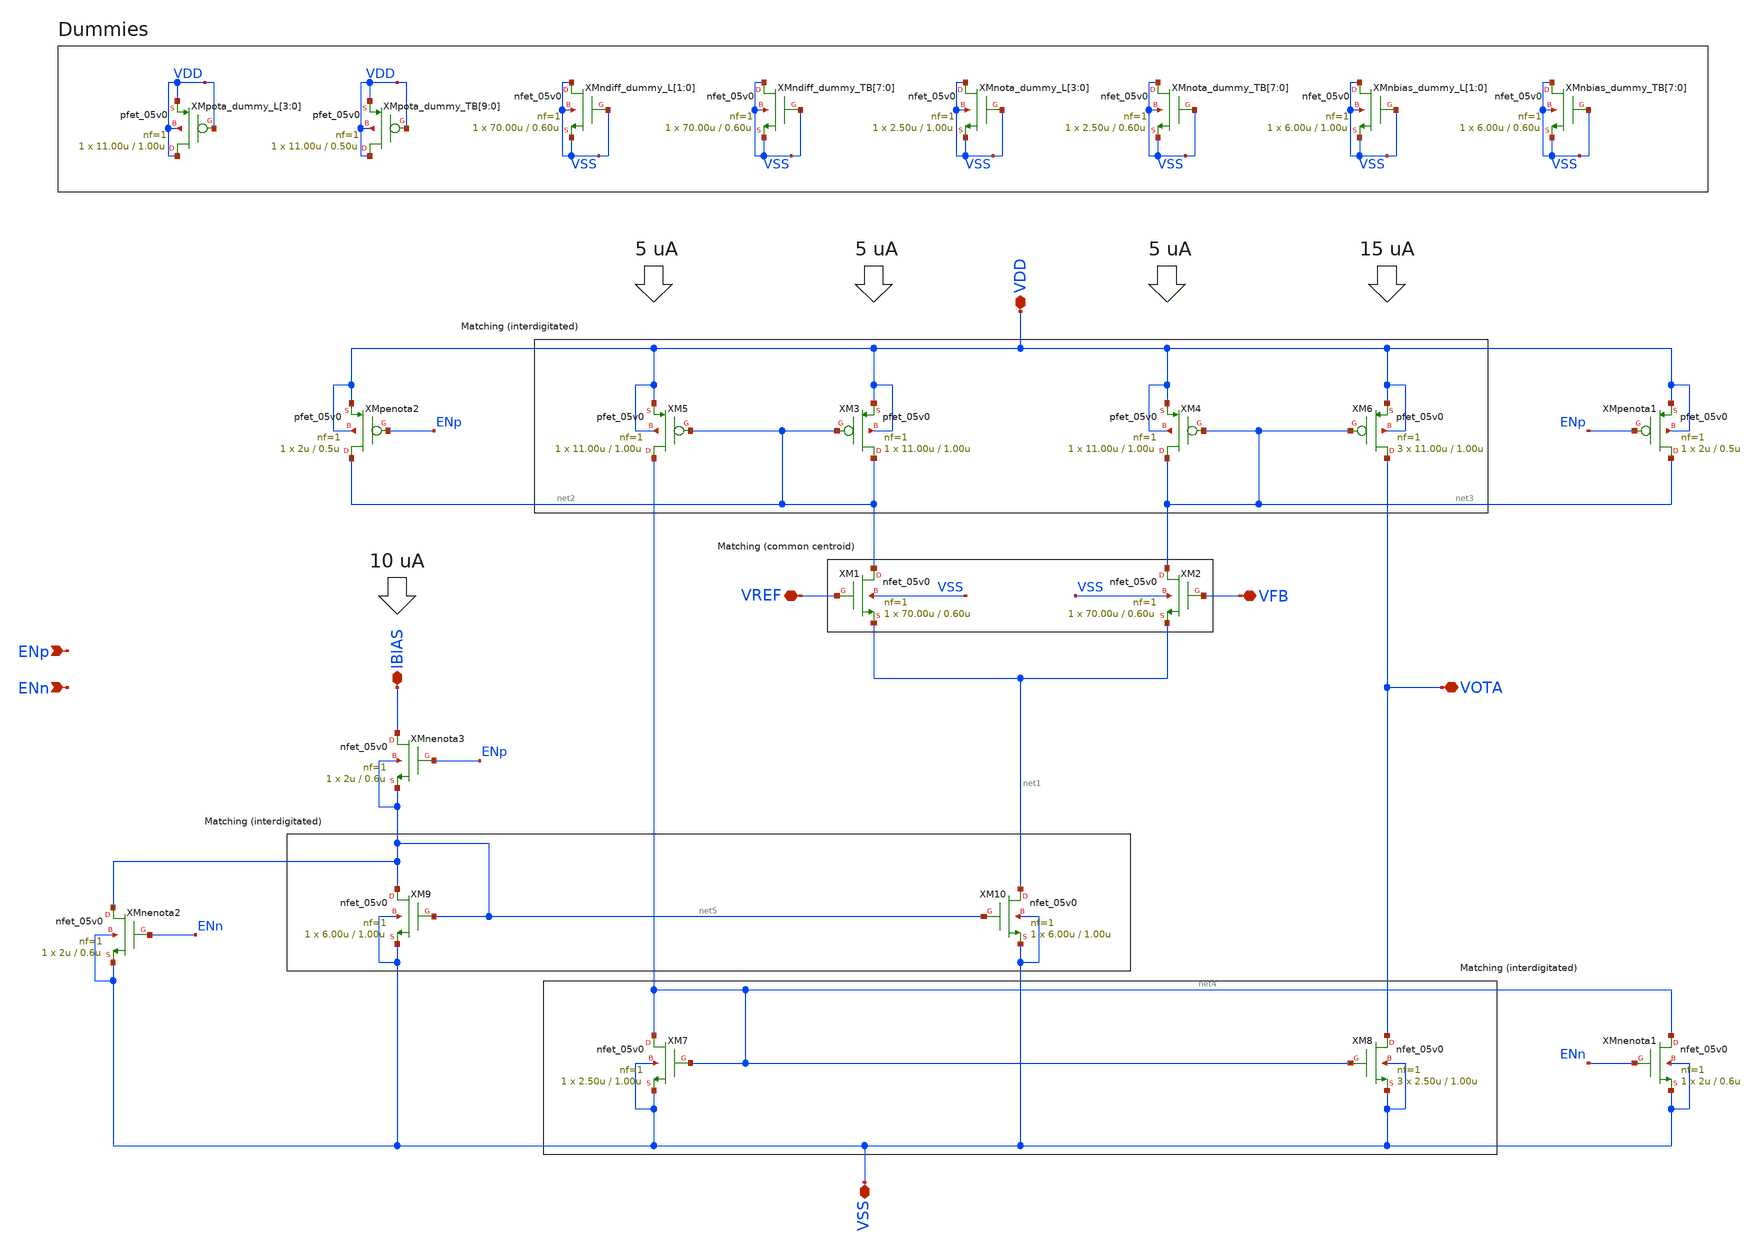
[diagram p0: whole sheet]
** sch_path: designs/libs/core_ldo/ldo_OTA/ldo_OTA.sch
**.subckt ldo_OTA VDD VSS VOTA VREF IBIAS VFB ENp ENn
*.iopin VDD
*.iopin VSS
*.iopin VOTA
*.iopin VREF
*.iopin IBIAS
*.iopin VFB
*.ipin ENp
*.ipin ENn
XM3 net2 net2 VDD VDD pfet_05v0 L=1.00u W=11.00u nf=1 ad='int((nf+1)/2) * W/nf * 0.18u' as='int((nf+2)/2) * W/nf * 0.18u'
+ pd='2*int((nf+1)/2) * (W/nf + 0.18u)' ps='2*int((nf+2)/2) * (W/nf + 0.18u)' nrd='0.18u / W' nrs='0.18u / W'
+ sa=0 sb=0 sd=0 m=1
XM4 net3 net3 VDD VDD pfet_05v0 L=1.00u W=11.00u nf=1 ad='int((nf+1)/2) * W/nf * 0.18u' as='int((nf+2)/2) * W/nf * 0.18u'
+ pd='2*int((nf+1)/2) * (W/nf + 0.18u)' ps='2*int((nf+2)/2) * (W/nf + 0.18u)' nrd='0.18u / W' nrs='0.18u / W'
+ sa=0 sb=0 sd=0 m=1
XM5 net4 net2 VDD VDD pfet_05v0 L=1.00u W=11.00u nf=1 ad='int((nf+1)/2) * W/nf * 0.18u' as='int((nf+2)/2) * W/nf * 0.18u'
+ pd='2*int((nf+1)/2) * (W/nf + 0.18u)' ps='2*int((nf+2)/2) * (W/nf + 0.18u)' nrd='0.18u / W' nrs='0.18u / W'
+ sa=0 sb=0 sd=0 m=1
XM6 VOTA net3 VDD VDD pfet_05v0 L=1.00u W=11.00u nf=1 ad='int((nf+1)/2) * W/nf * 0.18u' as='int((nf+2)/2) * W/nf * 0.18u'
+ pd='2*int((nf+1)/2) * (W/nf + 0.18u)' ps='2*int((nf+2)/2) * (W/nf + 0.18u)' nrd='0.18u / W' nrs='0.18u / W'
+ sa=0 sb=0 sd=0 m=3
XM9 net5 net5 VSS VSS nfet_05v0 L=1.00u W=6.00u nf=1 ad='int((nf+1)/2) * W/nf * 0.18u' as='int((nf+2)/2) * W/nf * 0.18u'
+ pd='2*int((nf+1)/2) * (W/nf + 0.18u)' ps='2*int((nf+2)/2) * (W/nf + 0.18u)' nrd='0.18u / W' nrs='0.18u / W'
+ sa=0 sb=0 sd=0 m=1
XM10 net1 net5 VSS VSS nfet_05v0 L=1.00u W=6.00u nf=1 ad='int((nf+1)/2) * W/nf * 0.18u' as='int((nf+2)/2) * W/nf * 0.18u'
+ pd='2*int((nf+1)/2) * (W/nf + 0.18u)' ps='2*int((nf+2)/2) * (W/nf + 0.18u)' nrd='0.18u / W' nrs='0.18u / W'
+ sa=0 sb=0 sd=0 m=1
XM7 net4 net4 VSS VSS nfet_05v0 L=1.00u W=2.50u nf=1 ad='int((nf+1)/2) * W/nf * 0.18u' as='int((nf+2)/2) * W/nf * 0.18u'
+ pd='2*int((nf+1)/2) * (W/nf + 0.18u)' ps='2*int((nf+2)/2) * (W/nf + 0.18u)' nrd='0.18u / W' nrs='0.18u / W'
+ sa=0 sb=0 sd=0 m=1
XM8 VOTA net4 VSS VSS nfet_05v0 L=1.00u W=2.50u nf=1 ad='int((nf+1)/2) * W/nf * 0.18u' as='int((nf+2)/2) * W/nf * 0.18u'
+ pd='2*int((nf+1)/2) * (W/nf + 0.18u)' ps='2*int((nf+2)/2) * (W/nf + 0.18u)' nrd='0.18u / W' nrs='0.18u / W'
+ sa=0 sb=0 sd=0 m=3
XM1 net2 VREF net1 VSS nfet_05v0 L=0.60u W=70.00u nf=1 ad='int((nf+1)/2) * W/nf * 0.18u' as='int((nf+2)/2) * W/nf * 0.18u'
+ pd='2*int((nf+1)/2) * (W/nf + 0.18u)' ps='2*int((nf+2)/2) * (W/nf + 0.18u)' nrd='0.18u / W' nrs='0.18u / W'
+ sa=0 sb=0 sd=0 m=1
XM2 net3 VFB net1 VSS nfet_05v0 L=0.60u W=70.00u nf=1 ad='int((nf+1)/2) * W/nf * 0.18u' as='int((nf+2)/2) * W/nf * 0.18u'
+ pd='2*int((nf+1)/2) * (W/nf + 0.18u)' ps='2*int((nf+2)/2) * (W/nf + 0.18u)' nrd='0.18u / W' nrs='0.18u / W'
+ sa=0 sb=0 sd=0 m=1
XMpota_dummy_L[3] VDD VDD VDD VDD pfet_05v0 L=1.00u W=11.00u nf=1 ad='int((nf+1)/2) * W/nf * 0.18u' as='int((nf+2)/2) * W/nf * 0.18u'
+ pd='2*int((nf+1)/2) * (W/nf + 0.18u)' ps='2*int((nf+2)/2) * (W/nf + 0.18u)' nrd='0.18u / W' nrs='0.18u / W'
+ sa=0 sb=0 sd=0 m=1
XMpota_dummy_L[2] VDD VDD VDD VDD pfet_05v0 L=1.00u W=11.00u nf=1 ad='int((nf+1)/2) * W/nf * 0.18u' as='int((nf+2)/2) * W/nf * 0.18u'
+ pd='2*int((nf+1)/2) * (W/nf + 0.18u)' ps='2*int((nf+2)/2) * (W/nf + 0.18u)' nrd='0.18u / W' nrs='0.18u / W'
+ sa=0 sb=0 sd=0 m=1
XMpota_dummy_L[1] VDD VDD VDD VDD pfet_05v0 L=1.00u W=11.00u nf=1 ad='int((nf+1)/2) * W/nf * 0.18u' as='int((nf+2)/2) * W/nf * 0.18u'
+ pd='2*int((nf+1)/2) * (W/nf + 0.18u)' ps='2*int((nf+2)/2) * (W/nf + 0.18u)' nrd='0.18u / W' nrs='0.18u / W'
+ sa=0 sb=0 sd=0 m=1
XMpota_dummy_L[0] VDD VDD VDD VDD pfet_05v0 L=1.00u W=11.00u nf=1 ad='int((nf+1)/2) * W/nf * 0.18u' as='int((nf+2)/2) * W/nf * 0.18u'
+ pd='2*int((nf+1)/2) * (W/nf + 0.18u)' ps='2*int((nf+2)/2) * (W/nf + 0.18u)' nrd='0.18u / W' nrs='0.18u / W'
+ sa=0 sb=0 sd=0 m=1
XMpota_dummy_TB[9] VDD VDD VDD VDD pfet_05v0 L=0.50u W=11.00u nf=1 ad='int((nf+1)/2) * W/nf * 0.18u'
+ as='int((nf+2)/2) * W/nf * 0.18u' pd='2*int((nf+1)/2) * (W/nf + 0.18u)' ps='2*int((nf+2)/2) * (W/nf + 0.18u)'
+ nrd='0.18u / W' nrs='0.18u / W' sa=0 sb=0 sd=0 m=1
XMpota_dummy_TB[8] VDD VDD VDD VDD pfet_05v0 L=0.50u W=11.00u nf=1 ad='int((nf+1)/2) * W/nf * 0.18u'
+ as='int((nf+2)/2) * W/nf * 0.18u' pd='2*int((nf+1)/2) * (W/nf + 0.18u)' ps='2*int((nf+2)/2) * (W/nf + 0.18u)'
+ nrd='0.18u / W' nrs='0.18u / W' sa=0 sb=0 sd=0 m=1
XMpota_dummy_TB[7] VDD VDD VDD VDD pfet_05v0 L=0.50u W=11.00u nf=1 ad='int((nf+1)/2) * W/nf * 0.18u'
+ as='int((nf+2)/2) * W/nf * 0.18u' pd='2*int((nf+1)/2) * (W/nf + 0.18u)' ps='2*int((nf+2)/2) * (W/nf + 0.18u)'
+ nrd='0.18u / W' nrs='0.18u / W' sa=0 sb=0 sd=0 m=1
XMpota_dummy_TB[6] VDD VDD VDD VDD pfet_05v0 L=0.50u W=11.00u nf=1 ad='int((nf+1)/2) * W/nf * 0.18u'
+ as='int((nf+2)/2) * W/nf * 0.18u' pd='2*int((nf+1)/2) * (W/nf + 0.18u)' ps='2*int((nf+2)/2) * (W/nf + 0.18u)'
+ nrd='0.18u / W' nrs='0.18u / W' sa=0 sb=0 sd=0 m=1
XMpota_dummy_TB[5] VDD VDD VDD VDD pfet_05v0 L=0.50u W=11.00u nf=1 ad='int((nf+1)/2) * W/nf * 0.18u'
+ as='int((nf+2)/2) * W/nf * 0.18u' pd='2*int((nf+1)/2) * (W/nf + 0.18u)' ps='2*int((nf+2)/2) * (W/nf + 0.18u)'
+ nrd='0.18u / W' nrs='0.18u / W' sa=0 sb=0 sd=0 m=1
XMpota_dummy_TB[4] VDD VDD VDD VDD pfet_05v0 L=0.50u W=11.00u nf=1 ad='int((nf+1)/2) * W/nf * 0.18u'
+ as='int((nf+2)/2) * W/nf * 0.18u' pd='2*int((nf+1)/2) * (W/nf + 0.18u)' ps='2*int((nf+2)/2) * (W/nf + 0.18u)'
+ nrd='0.18u / W' nrs='0.18u / W' sa=0 sb=0 sd=0 m=1
XMpota_dummy_TB[3] VDD VDD VDD VDD pfet_05v0 L=0.50u W=11.00u nf=1 ad='int((nf+1)/2) * W/nf * 0.18u'
+ as='int((nf+2)/2) * W/nf * 0.18u' pd='2*int((nf+1)/2) * (W/nf + 0.18u)' ps='2*int((nf+2)/2) * (W/nf + 0.18u)'
+ nrd='0.18u / W' nrs='0.18u / W' sa=0 sb=0 sd=0 m=1
XMpota_dummy_TB[2] VDD VDD VDD VDD pfet_05v0 L=0.50u W=11.00u nf=1 ad='int((nf+1)/2) * W/nf * 0.18u'
+ as='int((nf+2)/2) * W/nf * 0.18u' pd='2*int((nf+1)/2) * (W/nf + 0.18u)' ps='2*int((nf+2)/2) * (W/nf + 0.18u)'
+ nrd='0.18u / W' nrs='0.18u / W' sa=0 sb=0 sd=0 m=1
XMpota_dummy_TB[1] VDD VDD VDD VDD pfet_05v0 L=0.50u W=11.00u nf=1 ad='int((nf+1)/2) * W/nf * 0.18u'
+ as='int((nf+2)/2) * W/nf * 0.18u' pd='2*int((nf+1)/2) * (W/nf + 0.18u)' ps='2*int((nf+2)/2) * (W/nf + 0.18u)'
+ nrd='0.18u / W' nrs='0.18u / W' sa=0 sb=0 sd=0 m=1
XMpota_dummy_TB[0] VDD VDD VDD VDD pfet_05v0 L=0.50u W=11.00u nf=1 ad='int((nf+1)/2) * W/nf * 0.18u'
+ as='int((nf+2)/2) * W/nf * 0.18u' pd='2*int((nf+1)/2) * (W/nf + 0.18u)' ps='2*int((nf+2)/2) * (W/nf + 0.18u)'
+ nrd='0.18u / W' nrs='0.18u / W' sa=0 sb=0 sd=0 m=1
XMndiff_dummy_L[1] VSS VSS VSS VSS nfet_05v0 L=0.60u W=70.00u nf=1 ad='int((nf+1)/2) * W/nf * 0.18u'
+ as='int((nf+2)/2) * W/nf * 0.18u' pd='2*int((nf+1)/2) * (W/nf + 0.18u)' ps='2*int((nf+2)/2) * (W/nf + 0.18u)'
+ nrd='0.18u / W' nrs='0.18u / W' sa=0 sb=0 sd=0 m=1
XMndiff_dummy_L[0] VSS VSS VSS VSS nfet_05v0 L=0.60u W=70.00u nf=1 ad='int((nf+1)/2) * W/nf * 0.18u'
+ as='int((nf+2)/2) * W/nf * 0.18u' pd='2*int((nf+1)/2) * (W/nf + 0.18u)' ps='2*int((nf+2)/2) * (W/nf + 0.18u)'
+ nrd='0.18u / W' nrs='0.18u / W' sa=0 sb=0 sd=0 m=1
XMndiff_dummy_TB[7] VSS VSS VSS VSS nfet_05v0 L=0.60u W=70.00u nf=1 ad='int((nf+1)/2) * W/nf * 0.18u'
+ as='int((nf+2)/2) * W/nf * 0.18u' pd='2*int((nf+1)/2) * (W/nf + 0.18u)' ps='2*int((nf+2)/2) * (W/nf + 0.18u)'
+ nrd='0.18u / W' nrs='0.18u / W' sa=0 sb=0 sd=0 m=1
XMndiff_dummy_TB[6] VSS VSS VSS VSS nfet_05v0 L=0.60u W=70.00u nf=1 ad='int((nf+1)/2) * W/nf * 0.18u'
+ as='int((nf+2)/2) * W/nf * 0.18u' pd='2*int((nf+1)/2) * (W/nf + 0.18u)' ps='2*int((nf+2)/2) * (W/nf + 0.18u)'
+ nrd='0.18u / W' nrs='0.18u / W' sa=0 sb=0 sd=0 m=1
XMndiff_dummy_TB[5] VSS VSS VSS VSS nfet_05v0 L=0.60u W=70.00u nf=1 ad='int((nf+1)/2) * W/nf * 0.18u'
+ as='int((nf+2)/2) * W/nf * 0.18u' pd='2*int((nf+1)/2) * (W/nf + 0.18u)' ps='2*int((nf+2)/2) * (W/nf + 0.18u)'
+ nrd='0.18u / W' nrs='0.18u / W' sa=0 sb=0 sd=0 m=1
XMndiff_dummy_TB[4] VSS VSS VSS VSS nfet_05v0 L=0.60u W=70.00u nf=1 ad='int((nf+1)/2) * W/nf * 0.18u'
+ as='int((nf+2)/2) * W/nf * 0.18u' pd='2*int((nf+1)/2) * (W/nf + 0.18u)' ps='2*int((nf+2)/2) * (W/nf + 0.18u)'
+ nrd='0.18u / W' nrs='0.18u / W' sa=0 sb=0 sd=0 m=1
XMndiff_dummy_TB[3] VSS VSS VSS VSS nfet_05v0 L=0.60u W=70.00u nf=1 ad='int((nf+1)/2) * W/nf * 0.18u'
+ as='int((nf+2)/2) * W/nf * 0.18u' pd='2*int((nf+1)/2) * (W/nf + 0.18u)' ps='2*int((nf+2)/2) * (W/nf + 0.18u)'
+ nrd='0.18u / W' nrs='0.18u / W' sa=0 sb=0 sd=0 m=1
XMndiff_dummy_TB[2] VSS VSS VSS VSS nfet_05v0 L=0.60u W=70.00u nf=1 ad='int((nf+1)/2) * W/nf * 0.18u'
+ as='int((nf+2)/2) * W/nf * 0.18u' pd='2*int((nf+1)/2) * (W/nf + 0.18u)' ps='2*int((nf+2)/2) * (W/nf + 0.18u)'
+ nrd='0.18u / W' nrs='0.18u / W' sa=0 sb=0 sd=0 m=1
XMndiff_dummy_TB[1] VSS VSS VSS VSS nfet_05v0 L=0.60u W=70.00u nf=1 ad='int((nf+1)/2) * W/nf * 0.18u'
+ as='int((nf+2)/2) * W/nf * 0.18u' pd='2*int((nf+1)/2) * (W/nf + 0.18u)' ps='2*int((nf+2)/2) * (W/nf + 0.18u)'
+ nrd='0.18u / W' nrs='0.18u / W' sa=0 sb=0 sd=0 m=1
XMndiff_dummy_TB[0] VSS VSS VSS VSS nfet_05v0 L=0.60u W=70.00u nf=1 ad='int((nf+1)/2) * W/nf * 0.18u'
+ as='int((nf+2)/2) * W/nf * 0.18u' pd='2*int((nf+1)/2) * (W/nf + 0.18u)' ps='2*int((nf+2)/2) * (W/nf + 0.18u)'
+ nrd='0.18u / W' nrs='0.18u / W' sa=0 sb=0 sd=0 m=1
XMnota_dummy_L[3] VSS VSS VSS VSS nfet_05v0 L=1.00u W=2.50u nf=1 ad='int((nf+1)/2) * W/nf * 0.18u' as='int((nf+2)/2) * W/nf * 0.18u'
+ pd='2*int((nf+1)/2) * (W/nf + 0.18u)' ps='2*int((nf+2)/2) * (W/nf + 0.18u)' nrd='0.18u / W' nrs='0.18u / W'
+ sa=0 sb=0 sd=0 m=1
XMnota_dummy_L[2] VSS VSS VSS VSS nfet_05v0 L=1.00u W=2.50u nf=1 ad='int((nf+1)/2) * W/nf * 0.18u' as='int((nf+2)/2) * W/nf * 0.18u'
+ pd='2*int((nf+1)/2) * (W/nf + 0.18u)' ps='2*int((nf+2)/2) * (W/nf + 0.18u)' nrd='0.18u / W' nrs='0.18u / W'
+ sa=0 sb=0 sd=0 m=1
XMnota_dummy_L[1] VSS VSS VSS VSS nfet_05v0 L=1.00u W=2.50u nf=1 ad='int((nf+1)/2) * W/nf * 0.18u' as='int((nf+2)/2) * W/nf * 0.18u'
+ pd='2*int((nf+1)/2) * (W/nf + 0.18u)' ps='2*int((nf+2)/2) * (W/nf + 0.18u)' nrd='0.18u / W' nrs='0.18u / W'
+ sa=0 sb=0 sd=0 m=1
XMnota_dummy_L[0] VSS VSS VSS VSS nfet_05v0 L=1.00u W=2.50u nf=1 ad='int((nf+1)/2) * W/nf * 0.18u' as='int((nf+2)/2) * W/nf * 0.18u'
+ pd='2*int((nf+1)/2) * (W/nf + 0.18u)' ps='2*int((nf+2)/2) * (W/nf + 0.18u)' nrd='0.18u / W' nrs='0.18u / W'
+ sa=0 sb=0 sd=0 m=1
XMnota_dummy_TB[7] VSS VSS VSS VSS nfet_05v0 L=0.60u W=2.50u nf=1 ad='int((nf+1)/2) * W/nf * 0.18u' as='int((nf+2)/2) * W/nf * 0.18u'
+ pd='2*int((nf+1)/2) * (W/nf + 0.18u)' ps='2*int((nf+2)/2) * (W/nf + 0.18u)' nrd='0.18u / W' nrs='0.18u / W'
+ sa=0 sb=0 sd=0 m=1
XMnota_dummy_TB[6] VSS VSS VSS VSS nfet_05v0 L=0.60u W=2.50u nf=1 ad='int((nf+1)/2) * W/nf * 0.18u' as='int((nf+2)/2) * W/nf * 0.18u'
+ pd='2*int((nf+1)/2) * (W/nf + 0.18u)' ps='2*int((nf+2)/2) * (W/nf + 0.18u)' nrd='0.18u / W' nrs='0.18u / W'
+ sa=0 sb=0 sd=0 m=1
XMnota_dummy_TB[5] VSS VSS VSS VSS nfet_05v0 L=0.60u W=2.50u nf=1 ad='int((nf+1)/2) * W/nf * 0.18u' as='int((nf+2)/2) * W/nf * 0.18u'
+ pd='2*int((nf+1)/2) * (W/nf + 0.18u)' ps='2*int((nf+2)/2) * (W/nf + 0.18u)' nrd='0.18u / W' nrs='0.18u / W'
+ sa=0 sb=0 sd=0 m=1
XMnota_dummy_TB[4] VSS VSS VSS VSS nfet_05v0 L=0.60u W=2.50u nf=1 ad='int((nf+1)/2) * W/nf * 0.18u' as='int((nf+2)/2) * W/nf * 0.18u'
+ pd='2*int((nf+1)/2) * (W/nf + 0.18u)' ps='2*int((nf+2)/2) * (W/nf + 0.18u)' nrd='0.18u / W' nrs='0.18u / W'
+ sa=0 sb=0 sd=0 m=1
XMnota_dummy_TB[3] VSS VSS VSS VSS nfet_05v0 L=0.60u W=2.50u nf=1 ad='int((nf+1)/2) * W/nf * 0.18u' as='int((nf+2)/2) * W/nf * 0.18u'
+ pd='2*int((nf+1)/2) * (W/nf + 0.18u)' ps='2*int((nf+2)/2) * (W/nf + 0.18u)' nrd='0.18u / W' nrs='0.18u / W'
+ sa=0 sb=0 sd=0 m=1
XMnota_dummy_TB[2] VSS VSS VSS VSS nfet_05v0 L=0.60u W=2.50u nf=1 ad='int((nf+1)/2) * W/nf * 0.18u' as='int((nf+2)/2) * W/nf * 0.18u'
+ pd='2*int((nf+1)/2) * (W/nf + 0.18u)' ps='2*int((nf+2)/2) * (W/nf + 0.18u)' nrd='0.18u / W' nrs='0.18u / W'
+ sa=0 sb=0 sd=0 m=1
XMnota_dummy_TB[1] VSS VSS VSS VSS nfet_05v0 L=0.60u W=2.50u nf=1 ad='int((nf+1)/2) * W/nf * 0.18u' as='int((nf+2)/2) * W/nf * 0.18u'
+ pd='2*int((nf+1)/2) * (W/nf + 0.18u)' ps='2*int((nf+2)/2) * (W/nf + 0.18u)' nrd='0.18u / W' nrs='0.18u / W'
+ sa=0 sb=0 sd=0 m=1
XMnota_dummy_TB[0] VSS VSS VSS VSS nfet_05v0 L=0.60u W=2.50u nf=1 ad='int((nf+1)/2) * W/nf * 0.18u' as='int((nf+2)/2) * W/nf * 0.18u'
+ pd='2*int((nf+1)/2) * (W/nf + 0.18u)' ps='2*int((nf+2)/2) * (W/nf + 0.18u)' nrd='0.18u / W' nrs='0.18u / W'
+ sa=0 sb=0 sd=0 m=1
XMnbias_dummy_L[1] VSS VSS VSS VSS nfet_05v0 L=1.00u W=6.00u nf=1 ad='int((nf+1)/2) * W/nf * 0.18u' as='int((nf+2)/2) * W/nf * 0.18u'
+ pd='2*int((nf+1)/2) * (W/nf + 0.18u)' ps='2*int((nf+2)/2) * (W/nf + 0.18u)' nrd='0.18u / W' nrs='0.18u / W'
+ sa=0 sb=0 sd=0 m=1
XMnbias_dummy_L[0] VSS VSS VSS VSS nfet_05v0 L=1.00u W=6.00u nf=1 ad='int((nf+1)/2) * W/nf * 0.18u' as='int((nf+2)/2) * W/nf * 0.18u'
+ pd='2*int((nf+1)/2) * (W/nf + 0.18u)' ps='2*int((nf+2)/2) * (W/nf + 0.18u)' nrd='0.18u / W' nrs='0.18u / W'
+ sa=0 sb=0 sd=0 m=1
XMnbias_dummy_TB[7] VSS VSS VSS VSS nfet_05v0 L=0.60u W=6.00u nf=1 ad='int((nf+1)/2) * W/nf * 0.18u'
+ as='int((nf+2)/2) * W/nf * 0.18u' pd='2*int((nf+1)/2) * (W/nf + 0.18u)' ps='2*int((nf+2)/2) * (W/nf + 0.18u)'
+ nrd='0.18u / W' nrs='0.18u / W' sa=0 sb=0 sd=0 m=1
XMnbias_dummy_TB[6] VSS VSS VSS VSS nfet_05v0 L=0.60u W=6.00u nf=1 ad='int((nf+1)/2) * W/nf * 0.18u'
+ as='int((nf+2)/2) * W/nf * 0.18u' pd='2*int((nf+1)/2) * (W/nf + 0.18u)' ps='2*int((nf+2)/2) * (W/nf + 0.18u)'
+ nrd='0.18u / W' nrs='0.18u / W' sa=0 sb=0 sd=0 m=1
XMnbias_dummy_TB[5] VSS VSS VSS VSS nfet_05v0 L=0.60u W=6.00u nf=1 ad='int((nf+1)/2) * W/nf * 0.18u'
+ as='int((nf+2)/2) * W/nf * 0.18u' pd='2*int((nf+1)/2) * (W/nf + 0.18u)' ps='2*int((nf+2)/2) * (W/nf + 0.18u)'
+ nrd='0.18u / W' nrs='0.18u / W' sa=0 sb=0 sd=0 m=1
XMnbias_dummy_TB[4] VSS VSS VSS VSS nfet_05v0 L=0.60u W=6.00u nf=1 ad='int((nf+1)/2) * W/nf * 0.18u'
+ as='int((nf+2)/2) * W/nf * 0.18u' pd='2*int((nf+1)/2) * (W/nf + 0.18u)' ps='2*int((nf+2)/2) * (W/nf + 0.18u)'
+ nrd='0.18u / W' nrs='0.18u / W' sa=0 sb=0 sd=0 m=1
XMnbias_dummy_TB[3] VSS VSS VSS VSS nfet_05v0 L=0.60u W=6.00u nf=1 ad='int((nf+1)/2) * W/nf * 0.18u'
+ as='int((nf+2)/2) * W/nf * 0.18u' pd='2*int((nf+1)/2) * (W/nf + 0.18u)' ps='2*int((nf+2)/2) * (W/nf + 0.18u)'
+ nrd='0.18u / W' nrs='0.18u / W' sa=0 sb=0 sd=0 m=1
XMnbias_dummy_TB[2] VSS VSS VSS VSS nfet_05v0 L=0.60u W=6.00u nf=1 ad='int((nf+1)/2) * W/nf * 0.18u'
+ as='int((nf+2)/2) * W/nf * 0.18u' pd='2*int((nf+1)/2) * (W/nf + 0.18u)' ps='2*int((nf+2)/2) * (W/nf + 0.18u)'
+ nrd='0.18u / W' nrs='0.18u / W' sa=0 sb=0 sd=0 m=1
XMnbias_dummy_TB[1] VSS VSS VSS VSS nfet_05v0 L=0.60u W=6.00u nf=1 ad='int((nf+1)/2) * W/nf * 0.18u'
+ as='int((nf+2)/2) * W/nf * 0.18u' pd='2*int((nf+1)/2) * (W/nf + 0.18u)' ps='2*int((nf+2)/2) * (W/nf + 0.18u)'
+ nrd='0.18u / W' nrs='0.18u / W' sa=0 sb=0 sd=0 m=1
XMnbias_dummy_TB[0] VSS VSS VSS VSS nfet_05v0 L=0.60u W=6.00u nf=1 ad='int((nf+1)/2) * W/nf * 0.18u'
+ as='int((nf+2)/2) * W/nf * 0.18u' pd='2*int((nf+1)/2) * (W/nf + 0.18u)' ps='2*int((nf+2)/2) * (W/nf + 0.18u)'
+ nrd='0.18u / W' nrs='0.18u / W' sa=0 sb=0 sd=0 m=1
XMpenota1 net3 ENp VDD VDD pfet_05v0 L=0.5u W=2u nf=1 ad='int((nf+1)/2) * W/nf * 0.18u' as='int((nf+2)/2) * W/nf * 0.18u'
+ pd='2*int((nf+1)/2) * (W/nf + 0.18u)' ps='2*int((nf+2)/2) * (W/nf + 0.18u)' nrd='0.18u / W' nrs='0.18u / W'
+ sa=0 sb=0 sd=0 m=1
XMpenota2 net2 ENp VDD VDD pfet_05v0 L=0.5u W=2u nf=1 ad='int((nf+1)/2) * W/nf * 0.18u' as='int((nf+2)/2) * W/nf * 0.18u'
+ pd='2*int((nf+1)/2) * (W/nf + 0.18u)' ps='2*int((nf+2)/2) * (W/nf + 0.18u)' nrd='0.18u / W' nrs='0.18u / W'
+ sa=0 sb=0 sd=0 m=1
XMnenota1 net4 ENn VSS VSS nfet_05v0 L=0.6u W=2u nf=1 ad='int((nf+1)/2) * W/nf * 0.18u' as='int((nf+2)/2) * W/nf * 0.18u'
+ pd='2*int((nf+1)/2) * (W/nf + 0.18u)' ps='2*int((nf+2)/2) * (W/nf + 0.18u)' nrd='0.18u / W' nrs='0.18u / W'
+ sa=0 sb=0 sd=0 m=1
XMnenota2 net5 ENn VSS VSS nfet_05v0 L=0.6u W=2u nf=1 ad='int((nf+1)/2) * W/nf * 0.18u' as='int((nf+2)/2) * W/nf * 0.18u'
+ pd='2*int((nf+1)/2) * (W/nf + 0.18u)' ps='2*int((nf+2)/2) * (W/nf + 0.18u)' nrd='0.18u / W' nrs='0.18u / W'
+ sa=0 sb=0 sd=0 m=1
XMnenota3 IBIAS ENp net5 net5 nfet_05v0 L=0.6u W=2u nf=1 ad='int((nf+1)/2) * W/nf * 0.18u' as='int((nf+2)/2) * W/nf * 0.18u'
+ pd='2*int((nf+1)/2) * (W/nf + 0.18u)' ps='2*int((nf+2)/2) * (W/nf + 0.18u)' nrd='0.18u / W' nrs='0.18u / W'
+ sa=0 sb=0 sd=0 m=1
**.ends
.end
